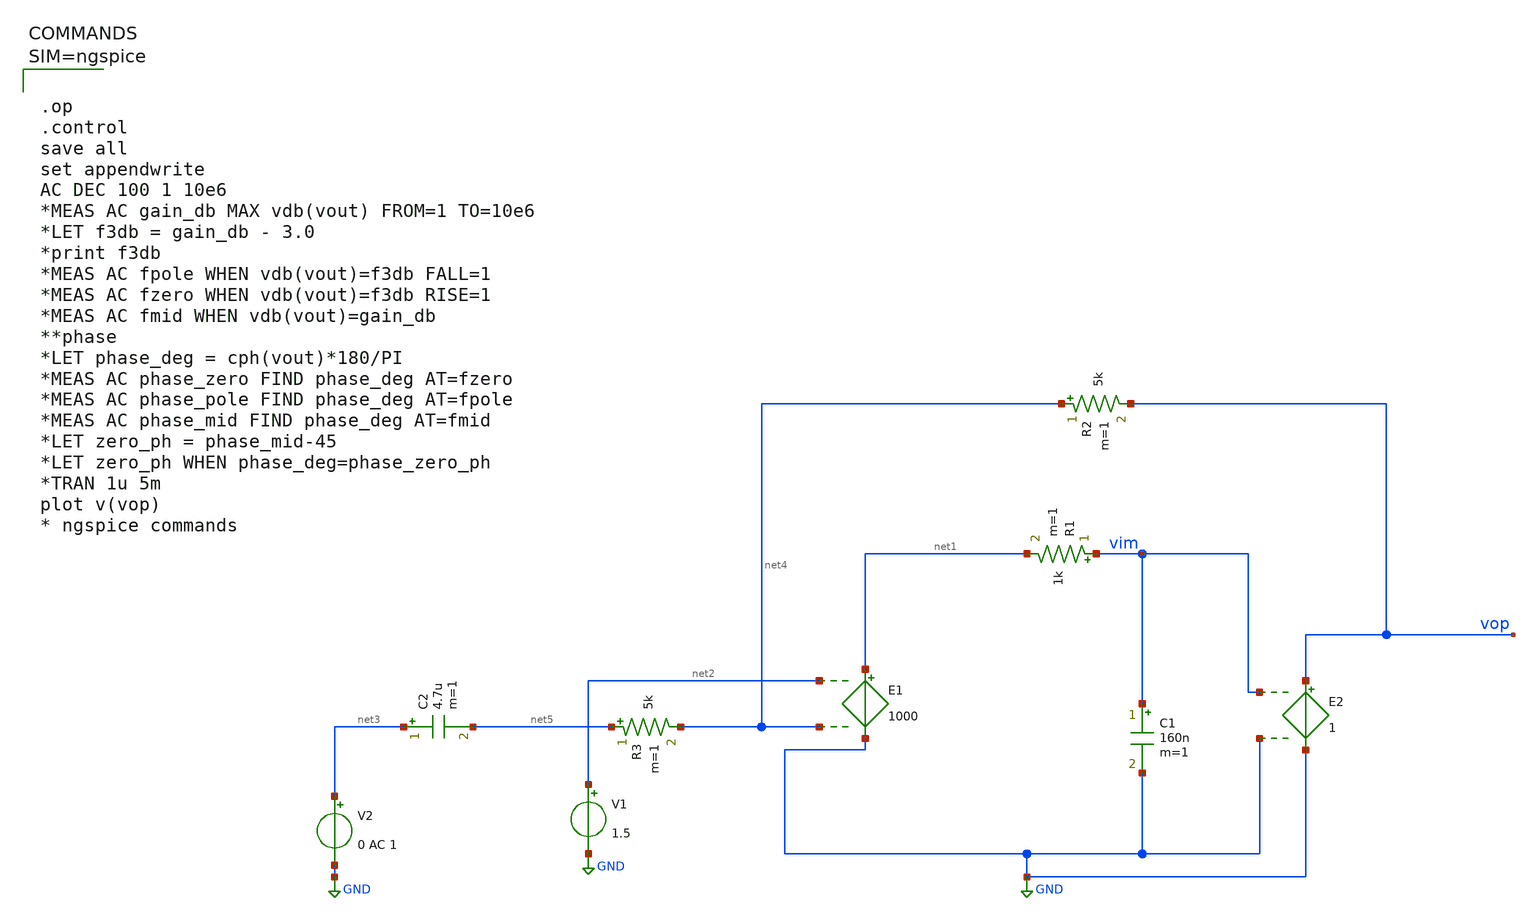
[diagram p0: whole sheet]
** sch_path: xschem/new_cascade-1.sch
**.subckt new_cascade-1
R1 vim net1 1k m=1
C1 vim GND 160n m=1
E1 net1 GND net2 net4 1000
E2 vop GND vim GND 1
V1 net2 GND 1.5
V2 net3 GND 0 AC 1
R2 net4 vop 5k m=1
R3 net5 net4 5k m=1
C2 net3 net5 4.7u m=1
**** begin user architecture code



.op
.control
save all
set appendwrite
AC DEC 100 1 10e6
*MEAS AC gain_db MAX vdb(vout) FROM=1 TO=10e6
*LET f3db = gain_db - 3.0
*print f3db
*MEAS AC fpole WHEN vdb(vout)=f3db FALL=1
*MEAS AC fzero WHEN vdb(vout)=f3db RISE=1
*MEAS AC fmid WHEN vdb(vout)=gain_db
**phase
*LET phase_deg = cph(vout)*180/PI
*MEAS AC phase_zero FIND phase_deg AT=fzero
*MEAS AC phase_pole FIND phase_deg AT=fpole
*MEAS AC phase_mid FIND phase_deg AT=fmid
*LET zero_ph = phase_mid-45
*LET zero_ph WHEN phase_deg=phase_zero_ph
*TRAN 1u 5m
plot v(vop)
* ngspice commands



**** end user architecture code
**.ends
.GLOBAL GND
.end
